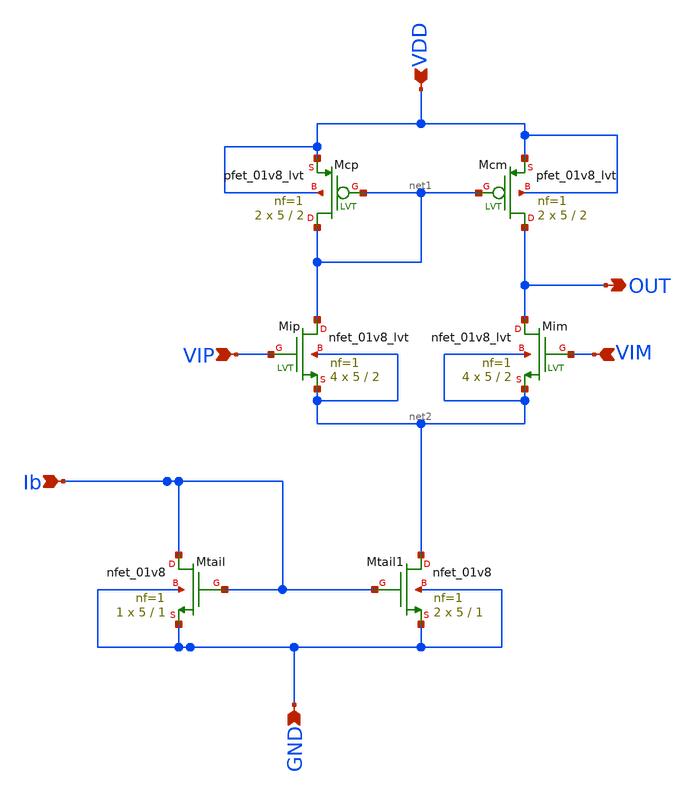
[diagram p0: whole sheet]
** sch_path: Work/xschem/nmos_diff_layout.sch
**.subckt nmos_diff_layout VIP VDD VIM Ib GND OUT
*.ipin VIP
*.ipin VDD
*.ipin VIM
*.ipin Ib
*.ipin GND
*.opin OUT
XMip net1 VIP net2 net2 sky130_fd_pr__nfet_01v8_lvt L=2 W=5 nf=1 ad='int((1 + 1)/2) * 5 / 1 * 0.29' as='int((1 + 2)/2) * 5 / 1 * 0.29'
+ pd='2*int((1 + 1)/2) * (5 / 1 + 0.29)' ps='2*int((1 + 2)/2) * (5 / 1 + 0.29)' nrd='0.29 / 5 ' nrs='0.29 / 5 '
+ sa=0 sb=0 sd=0 mult=4 m=4
XMim OUT VIM net2 net2 sky130_fd_pr__nfet_01v8_lvt L=2 W=5 nf=1 ad='int((1 + 1)/2) * 5 / 1 * 0.29' as='int((1 + 2)/2) * 5 / 1 * 0.29'
+ pd='2*int((1 + 1)/2) * (5 / 1 + 0.29)' ps='2*int((1 + 2)/2) * (5 / 1 + 0.29)' nrd='0.29 / 5 ' nrs='0.29 / 5 '
+ sa=0 sb=0 sd=0 mult=4 m=4
XMcp net1 net1 VDD VDD sky130_fd_pr__pfet_01v8_lvt L=2 W=5 nf=1 ad='int((1 + 1)/2) * 5 / 1 * 0.29' as='int((1 + 2)/2) * 5 / 1 * 0.29'
+ pd='2*int((1 + 1)/2) * (5 / 1 + 0.29)' ps='2*int((1 + 2)/2) * (5 / 1 + 0.29)' nrd='0.29 / 5 ' nrs='0.29 / 5 '
+ sa=0 sb=0 sd=0 mult=2 m=2
XMcm OUT net1 VDD VDD sky130_fd_pr__pfet_01v8_lvt L=2 W=5 nf=1 ad='int((1 + 1)/2) * 5 / 1 * 0.29' as='int((1 + 2)/2) * 5 / 1 * 0.29'
+ pd='2*int((1 + 1)/2) * (5 / 1 + 0.29)' ps='2*int((1 + 2)/2) * (5 / 1 + 0.29)' nrd='0.29 / 5 ' nrs='0.29 / 5 '
+ sa=0 sb=0 sd=0 mult=2 m=2
XMtail Ib Ib GND GND sky130_fd_pr__nfet_01v8 L=1 W=5 nf=1 ad='int((1 + 1)/2) * 5 / 1 * 0.29' as='int((1 + 2)/2) * 5 / 1 * 0.29'
+ pd='2*int((1 + 1)/2) * (5 / 1 + 0.29)' ps='2*int((1 + 2)/2) * (5 / 1 + 0.29)' nrd='0.29 / 5 ' nrs='0.29 / 5 '
+ sa=0 sb=0 sd=0 mult=1 m=1
XMtail1 net2 Ib GND GND sky130_fd_pr__nfet_01v8 L=1 W=5 nf=1 ad='int((1 + 1)/2) * 5 / 1 * 0.29' as='int((1 + 2)/2) * 5 / 1 * 0.29'
+ pd='2*int((1 + 1)/2) * (5 / 1 + 0.29)' ps='2*int((1 + 2)/2) * (5 / 1 + 0.29)' nrd='0.29 / 5 ' nrs='0.29 / 5 '
+ sa=0 sb=0 sd=0 mult=2 m=2
**** begin user architecture code
.lib /usr/local/share/pdk/sky130A/libs.tech/ngspice/sky130.lib.spice tt
**** end user architecture code
**.ends
.end
